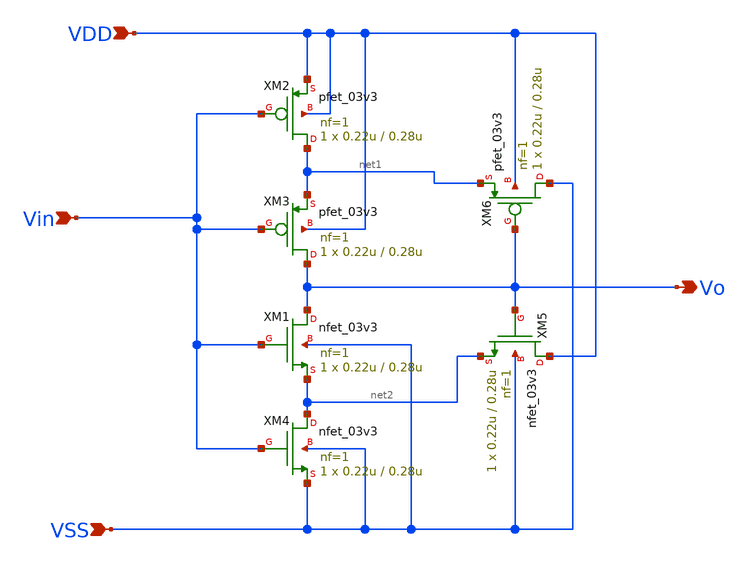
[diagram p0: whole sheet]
** sch_path: designs/Schmitt.sch
**.subckt Schmitt VDD VSS Vin Vo
*.ipin VDD
*.ipin VSS
*.ipin Vin
*.opin Vo
XM1 Vo Vin net2 VSS nfet_03v3 L=0.28u W=0.22u nf=1 ad='int((nf+1)/2) * W/nf * 0.18u' as='int((nf+2)/2) * W/nf * 0.18u'
+ pd='2*int((nf+1)/2) * (W/nf + 0.18u)' ps='2*int((nf+2)/2) * (W/nf + 0.18u)' nrd='0.18u / W' nrs='0.18u / W'
+ sa=0 sb=0 sd=0 m=1
XM2 net1 Vin VDD VDD pfet_03v3 L=0.28u W=0.22u nf=1 ad='int((nf+1)/2) * W/nf * 0.18u' as='int((nf+2)/2) * W/nf * 0.18u'
+ pd='2*int((nf+1)/2) * (W/nf + 0.18u)' ps='2*int((nf+2)/2) * (W/nf + 0.18u)' nrd='0.18u / W' nrs='0.18u / W'
+ sa=0 sb=0 sd=0 m=1
XM3 Vo Vin net1 VDD pfet_03v3 L=0.28u W=0.22u nf=1 ad='int((nf+1)/2) * W/nf * 0.18u' as='int((nf+2)/2) * W/nf * 0.18u'
+ pd='2*int((nf+1)/2) * (W/nf + 0.18u)' ps='2*int((nf+2)/2) * (W/nf + 0.18u)' nrd='0.18u / W' nrs='0.18u / W'
+ sa=0 sb=0 sd=0 m=1
XM4 net2 Vin VSS VSS nfet_03v3 L=0.28u W=0.22u nf=1 ad='int((nf+1)/2) * W/nf * 0.18u' as='int((nf+2)/2) * W/nf * 0.18u'
+ pd='2*int((nf+1)/2) * (W/nf + 0.18u)' ps='2*int((nf+2)/2) * (W/nf + 0.18u)' nrd='0.18u / W' nrs='0.18u / W'
+ sa=0 sb=0 sd=0 m=1
XM5 VDD Vo net2 VSS nfet_03v3 L=0.28u W=0.22u nf=1 ad='int((nf+1)/2) * W/nf * 0.18u' as='int((nf+2)/2) * W/nf * 0.18u'
+ pd='2*int((nf+1)/2) * (W/nf + 0.18u)' ps='2*int((nf+2)/2) * (W/nf + 0.18u)' nrd='0.18u / W' nrs='0.18u / W'
+ sa=0 sb=0 sd=0 m=1
XM6 VSS Vo net1 VDD pfet_03v3 L=0.28u W=0.22u nf=1 ad='int((nf+1)/2) * W/nf * 0.18u' as='int((nf+2)/2) * W/nf * 0.18u'
+ pd='2*int((nf+1)/2) * (W/nf + 0.18u)' ps='2*int((nf+2)/2) * (W/nf + 0.18u)' nrd='0.18u / W' nrs='0.18u / W'
+ sa=0 sb=0 sd=0 m=1
**.ends
.end
